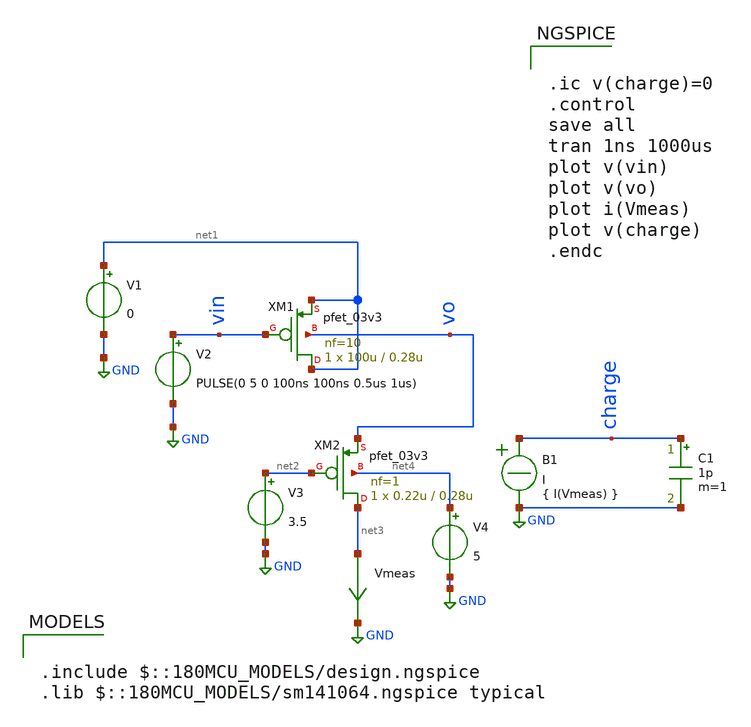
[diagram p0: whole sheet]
** sch_path: xschem/interface_trap_charge_pump_cascode.sch
**.subckt interface_trap_charge_pump_cascode
XM1 net1 vin net1 vo pfet_03v3 L=0.28u W=100u nf=10 ad='int((nf+1)/2) * W/nf * 0.18u' as='int((nf+2)/2) * W/nf * 0.18u'
+ pd='2*int((nf+1)/2) * (W/nf + 0.18u)' ps='2*int((nf+2)/2) * (W/nf + 0.18u)' nrd='0.18u / W' nrs='0.18u / W'
+ sa=0 sb=0 sd=0 m=1
V1 net1 GND 0
Vmeas net3 GND 0
.save i(vmeas)
V2 vin GND PULSE(0 5 0 100ns 100ns 0.5us 1us)
V3 net2 GND 3.5
B1 charge GND I = { I(Vmeas) }
C1 charge GND 1p m=1
XM2 net3 net2 vo net4 pfet_03v3 L=0.28u W=0.22u nf=1 ad='int((nf+1)/2) * W/nf * 0.18u' as='int((nf+2)/2) * W/nf * 0.18u'
+ pd='2*int((nf+1)/2) * (W/nf + 0.18u)' ps='2*int((nf+2)/2) * (W/nf + 0.18u)' nrd='0.18u / W' nrs='0.18u / W'
+ sa=0 sb=0 sd=0 m=1
V4 net4 GND 5
**** begin user architecture code


.ic v(charge)=0
.control
save all
tran 1ns 1000us
plot v(vin)
plot v(vo)
plot i(Vmeas)
plot v(charge)
.endc



.include $::180MCU_MODELS/design.ngspice
.lib $::180MCU_MODELS/sm141064.ngspice typical

**** end user architecture code
**.ends
.GLOBAL GND
.end
